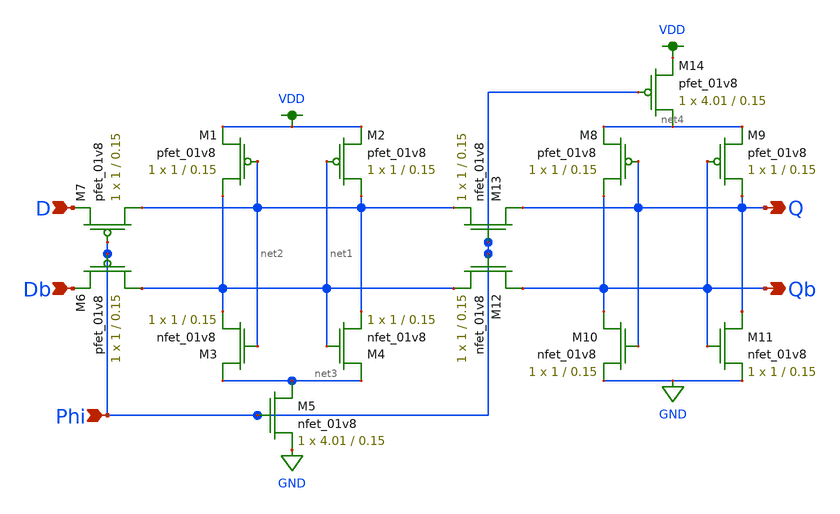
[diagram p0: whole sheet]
** sch_path: mp2/latch.sch
**.subckt latch D Db Q Qb Phi
*.ipin D
*.ipin Db
*.opin Q
*.opin Qb
*.ipin Phi
XM1 net1 net2 VDD VDD sky130_fd_pr__pfet_01v8 L=0.15 W=1 nf=1 ad='int((nf+1)/2) * W/nf * 0.29' as='int((nf+2)/2) * W/nf * 0.29'
+ pd='2*int((nf+1)/2) * (W/nf + 0.29)' ps='2*int((nf+2)/2) * (W/nf + 0.29)' nrd='0.29 / W' nrs='0.29 / W'
+ sa=0 sb=0 sd=0 mult=1 m=1
XM2 net2 net1 VDD VDD sky130_fd_pr__pfet_01v8 L=0.15 W=1 nf=1 ad='int((nf+1)/2) * W/nf * 0.29' as='int((nf+2)/2) * W/nf * 0.29'
+ pd='2*int((nf+1)/2) * (W/nf + 0.29)' ps='2*int((nf+2)/2) * (W/nf + 0.29)' nrd='0.29 / W' nrs='0.29 / W'
+ sa=0 sb=0 sd=0 mult=1 m=1
XM3 net3 net2 net1 GND sky130_fd_pr__nfet_01v8 L=0.15 W=1 nf=1 ad='int((nf+1)/2) * W/nf * 0.29' as='int((nf+2)/2) * W/nf * 0.29'
+ pd='2*int((nf+1)/2) * (W/nf + 0.29)' ps='2*int((nf+2)/2) * (W/nf + 0.29)' nrd='0.29 / W' nrs='0.29 / W'
+ sa=0 sb=0 sd=0 mult=1 m=1
XM4 net3 net1 net2 GND sky130_fd_pr__nfet_01v8 L=0.15 W=1 nf=1 ad='int((nf+1)/2) * W/nf * 0.29' as='int((nf+2)/2) * W/nf * 0.29'
+ pd='2*int((nf+1)/2) * (W/nf + 0.29)' ps='2*int((nf+2)/2) * (W/nf + 0.29)' nrd='0.29 / W' nrs='0.29 / W'
+ sa=0 sb=0 sd=0 mult=1 m=1
XM5 net3 Phi GND GND sky130_fd_pr__nfet_01v8 L=0.15 W=4.01 nf=1 ad='int((nf+1)/2) * W/nf * 0.29' as='int((nf+2)/2) * W/nf * 0.29'
+ pd='2*int((nf+1)/2) * (W/nf + 0.29)' ps='2*int((nf+2)/2) * (W/nf + 0.29)' nrd='0.29 / W' nrs='0.29 / W'
+ sa=0 sb=0 sd=0 mult=1 m=1
XM6 net1 Phi Db VDD sky130_fd_pr__pfet_01v8 L=0.15 W=1 nf=1 ad='int((nf+1)/2) * W/nf * 0.29' as='int((nf+2)/2) * W/nf * 0.29'
+ pd='2*int((nf+1)/2) * (W/nf + 0.29)' ps='2*int((nf+2)/2) * (W/nf + 0.29)' nrd='0.29 / W' nrs='0.29 / W'
+ sa=0 sb=0 sd=0 mult=1 m=1
XM7 net2 Phi D VDD sky130_fd_pr__pfet_01v8 L=0.15 W=1 nf=1 ad='int((nf+1)/2) * W/nf * 0.29' as='int((nf+2)/2) * W/nf * 0.29'
+ pd='2*int((nf+1)/2) * (W/nf + 0.29)' ps='2*int((nf+2)/2) * (W/nf + 0.29)' nrd='0.29 / W' nrs='0.29 / W'
+ sa=0 sb=0 sd=0 mult=1 m=1
XM8 Qb Q net4 VDD sky130_fd_pr__pfet_01v8 L=0.15 W=1 nf=1 ad='int((nf+1)/2) * W/nf * 0.29' as='int((nf+2)/2) * W/nf * 0.29'
+ pd='2*int((nf+1)/2) * (W/nf + 0.29)' ps='2*int((nf+2)/2) * (W/nf + 0.29)' nrd='0.29 / W' nrs='0.29 / W'
+ sa=0 sb=0 sd=0 mult=1 m=1
XM9 Q Qb net4 VDD sky130_fd_pr__pfet_01v8 L=0.15 W=1 nf=1 ad='int((nf+1)/2) * W/nf * 0.29' as='int((nf+2)/2) * W/nf * 0.29'
+ pd='2*int((nf+1)/2) * (W/nf + 0.29)' ps='2*int((nf+2)/2) * (W/nf + 0.29)' nrd='0.29 / W' nrs='0.29 / W'
+ sa=0 sb=0 sd=0 mult=1 m=1
XM10 Qb Q GND GND sky130_fd_pr__nfet_01v8 L=0.15 W=1 nf=1 ad='int((nf+1)/2) * W/nf * 0.29' as='int((nf+2)/2) * W/nf * 0.29'
+ pd='2*int((nf+1)/2) * (W/nf + 0.29)' ps='2*int((nf+2)/2) * (W/nf + 0.29)' nrd='0.29 / W' nrs='0.29 / W'
+ sa=0 sb=0 sd=0 mult=1 m=1
XM11 Q Qb GND GND sky130_fd_pr__nfet_01v8 L=0.15 W=1 nf=1 ad='int((nf+1)/2) * W/nf * 0.29' as='int((nf+2)/2) * W/nf * 0.29'
+ pd='2*int((nf+1)/2) * (W/nf + 0.29)' ps='2*int((nf+2)/2) * (W/nf + 0.29)' nrd='0.29 / W' nrs='0.29 / W'
+ sa=0 sb=0 sd=0 mult=1 m=1
XM12 Qb Phi net1 GND sky130_fd_pr__nfet_01v8 L=0.15 W=1 nf=1 ad='int((nf+1)/2) * W/nf * 0.29' as='int((nf+2)/2) * W/nf * 0.29'
+ pd='2*int((nf+1)/2) * (W/nf + 0.29)' ps='2*int((nf+2)/2) * (W/nf + 0.29)' nrd='0.29 / W' nrs='0.29 / W'
+ sa=0 sb=0 sd=0 mult=1 m=1
XM13 Q Phi net2 GND sky130_fd_pr__nfet_01v8 L=0.15 W=1 nf=1 ad='int((nf+1)/2) * W/nf * 0.29' as='int((nf+2)/2) * W/nf * 0.29'
+ pd='2*int((nf+1)/2) * (W/nf + 0.29)' ps='2*int((nf+2)/2) * (W/nf + 0.29)' nrd='0.29 / W' nrs='0.29 / W'
+ sa=0 sb=0 sd=0 mult=1 m=1
XM14 net4 Phi VDD VDD sky130_fd_pr__pfet_01v8 L=0.15 W=4.01 nf=1 ad='int((nf+1)/2) * W/nf * 0.29' as='int((nf+2)/2) * W/nf * 0.29'
+ pd='2*int((nf+1)/2) * (W/nf + 0.29)' ps='2*int((nf+2)/2) * (W/nf + 0.29)' nrd='0.29 / W' nrs='0.29 / W'
+ sa=0 sb=0 sd=0 mult=1 m=1
**.ends
.GLOBAL GND
.GLOBAL VDD
.end
